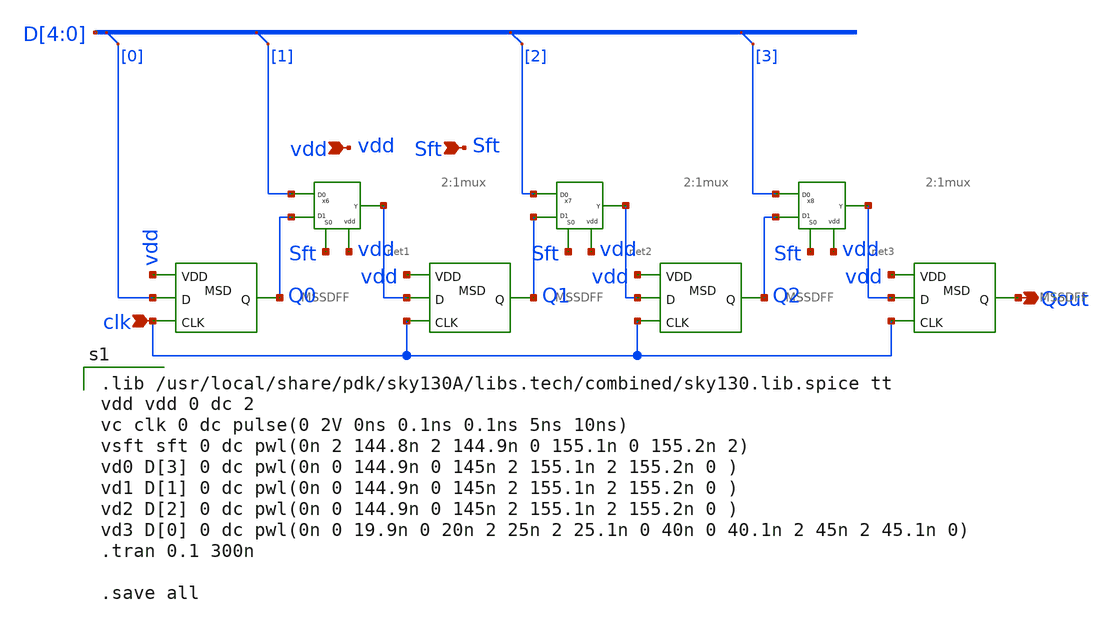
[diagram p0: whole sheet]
** sch_path: Circuit Files/circuits/circuits/AIOSR.sch
**.subckt AIOSR Qout vdd clk Sft
*.opin Qout
*.ipin vdd
*.ipin clk
*.ipin Sft
x1 Q0 vdd D[0] clk MSSDFF
x2 Q1 vdd net1 clk MSSDFF
x3 Q2 vdd net2 clk MSSDFF
x4 Qout vdd net3 clk MSSDFF
x6 D[1] Sft vdd net1 Q0 2:1mux
x7 D[2] Sft vdd net2 Q1 2:1mux
x8 D[3] Sft vdd net3 Q2 2:1mux
* tap: D[4:0] --> D[0]
* tap: D[4:0] --> D[1]
* tap: D[4:0] --> D[2]
* tap: D[4:0] --> D[3]
**** begin user architecture code

.lib /usr/local/share/pdk/sky130A/libs.tech/combined/sky130.lib.spice tt
vdd vdd 0 dc 2
vc clk 0 dc pulse(0 2V 0ns 0.1ns 0.1ns 5ns 10ns)
vsft sft 0 dc pwl(0n 2 144.8n 2 144.9n 0 155.1n 0 155.2n 2)
vd0 D[3] 0 dc pwl(0n 0 144.9n 0 145n 2 155.1n 2 155.2n 0 )
vd1 D[1] 0 dc pwl(0n 0 144.9n 0 145n 2 155.1n 2 155.2n 0 )
vd2 D[2] 0 dc pwl(0n 0 144.9n 0 145n 2 155.1n 2 155.2n 0 )
vd3 D[0] 0 dc pwl(0n 0 19.9n 0 20n 2 25n 2 25.1n 0 40n 0 40.1n 2 45n 2 45.1n 0)
.tran 0.1 300n

.save all


**** end user architecture code
**.ends

* expanding   symbol:  daVLSI_World/circuits/MSSDFF.sym # of pins=4
** sym_path: Circuit Files/circuits/circuits/MSSDFF.sym
** sch_path: Circuit Files/circuits/circuits/MSSDFF.sch
.subckt MSSDFF Q VDD D CLK
*.ipin D
*.opin Q
*.ipin CLK
*.ipin VDD
x2 VDD D net2 CLK DFF1
x1 VDD net2 Q net1 DFF1
x3 net3 net4 net5 inverter_vtc
.ends


* expanding   symbol:  daVLSI_World/circuits/2:1mux.sym # of pins=5
** sym_path: Circuit Files/circuits/circuits/2:1mux.sym
** sch_path: Circuit Files/circuits/circuits/2:1mux.sch
.subckt 2:1mux D0 S0 vdd Y D1
*.ipin vdd
*.ipin D1
*.ipin D0
*.ipin S0
*.opin Y
x1 vdd net3 net1 D0 AND_gate
x2 vdd net1 net2 Y OR_gate
x3 vdd net4 net5 inverter_vtc
x4 vdd S0 net2 D1 AND_gate
.ends


* expanding   symbol:  daVLSI_World/circuits/DFF1.sym # of pins=4
** sym_path: Circuit Files/circuits/circuits/DFF1.sym
** sch_path: Circuit Files/circuits/circuits/DFF1.sch
.subckt DFF1 vdd D Q clk
*.ipin clk
*.ipin D
*.ipin vdd
*.opin Q
x1 vdd net3 D clk GND NAND_gate
x3 vdd Q net3 net1 GND NAND_gate
x4 vdd net4 clk net2 GND NAND_gate
x5 vdd net1 Q net4 GND NAND_gate
x9 net5 net6 net7 inverter_vtc
**** begin user architecture code


.IC V(Q)=0


**** end user architecture code
.ends


* expanding   symbol:  daVLSI_World/gates/inverter_vtc.sym # of pins=3
** sym_path: Circuit Files/Logic gate design using MOSFETS/gates/inverter_vtc.sym
** sch_path: Circuit Files/Logic gate design using MOSFETS/gates/inverter_vtc.sch
.subckt inverter_vtc vdd vin vout
*.ipin vin
*.opin vout
*.ipin vdd
XM1 vout vin GND GND sky130_fd_pr__nfet_01v8 L=0.15 W=1 nf=1 ad='int((nf+1)/2) * W/nf * 0.29' as='int((nf+2)/2) * W/nf * 0.29'
+ pd='2*int((nf+1)/2) * (W/nf + 0.29)' ps='2*int((nf+2)/2) * (W/nf + 0.29)' nrd='0.29 / W' nrs='0.29 / W'
+ sa=0 sb=0 sd=0 mult=1 m=1
XM2 vout vin vdd vdd sky130_fd_pr__pfet_01v8 L=0.15 W=2 nf=1 ad='int((nf+1)/2) * W/nf * 0.29' as='int((nf+2)/2) * W/nf * 0.29'
+ pd='2*int((nf+1)/2) * (W/nf + 0.29)' ps='2*int((nf+2)/2) * (W/nf + 0.29)' nrd='0.29 / W' nrs='0.29 / W'
+ sa=0 sb=0 sd=0 mult=1 m=1
.ends


* expanding   symbol:  daVLSI_World/gates/AND_gate.sym # of pins=4
** sym_path: Circuit Files/Logic gate design using MOSFETS/gates/AND_gate.sym
** sch_path: Circuit Files/Logic gate design using MOSFETS/gates/AND_gate.sch
.subckt AND_gate vdd A Y B
*.opin Y
*.ipin A
*.ipin B
*.ipin vdd
x1 vdd net1 A B GND NAND_gate
x2 vdd net1 Y inverter_vtc
.ends


* expanding   symbol:  daVLSI_World/gates/OR_gate.sym # of pins=4
** sym_path: Circuit Files/Logic gate design using MOSFETS/gates/OR_gate.sym
** sch_path: Circuit Files/Logic gate design using MOSFETS/gates/OR_gate.sch
.subckt OR_gate vdd A B Y
*.ipin A
*.ipin B
*.ipin vdd
*.opin Y
XM1 net1 B net2 vdd sky130_fd_pr__pfet_01v8 L=0.15 W=2 nf=1 ad='int((nf+1)/2) * W/nf * 0.29' as='int((nf+2)/2) * W/nf * 0.29'
+ pd='2*int((nf+1)/2) * (W/nf + 0.29)' ps='2*int((nf+2)/2) * (W/nf + 0.29)' nrd='0.29 / W' nrs='0.29 / W'
+ sa=0 sb=0 sd=0 mult=1 m=1
XM2 net2 A vdd vdd sky130_fd_pr__pfet_01v8 L=0.15 W=2 nf=1 ad='int((nf+1)/2) * W/nf * 0.29' as='int((nf+2)/2) * W/nf * 0.29'
+ pd='2*int((nf+1)/2) * (W/nf + 0.29)' ps='2*int((nf+2)/2) * (W/nf + 0.29)' nrd='0.29 / W' nrs='0.29 / W'
+ sa=0 sb=0 sd=0 mult=1 m=1
XM3 net1 B GND GND sky130_fd_pr__nfet_01v8 L=0.15 W=1 nf=1 ad='int((nf+1)/2) * W/nf * 0.29' as='int((nf+2)/2) * W/nf * 0.29'
+ pd='2*int((nf+1)/2) * (W/nf + 0.29)' ps='2*int((nf+2)/2) * (W/nf + 0.29)' nrd='0.29 / W' nrs='0.29 / W'
+ sa=0 sb=0 sd=0 mult=1 m=1
XM4 net1 A GND GND sky130_fd_pr__nfet_01v8 L=0.15 W=1 nf=1 ad='int((nf+1)/2) * W/nf * 0.29' as='int((nf+2)/2) * W/nf * 0.29'
+ pd='2*int((nf+1)/2) * (W/nf + 0.29)' ps='2*int((nf+2)/2) * (W/nf + 0.29)' nrd='0.29 / W' nrs='0.29 / W'
+ sa=0 sb=0 sd=0 mult=1 m=1
XM9 Y net1 vdd vdd sky130_fd_pr__pfet_01v8 L=0.15 W=2 nf=1 ad='int((nf+1)/2) * W/nf * 0.29' as='int((nf+2)/2) * W/nf * 0.29'
+ pd='2*int((nf+1)/2) * (W/nf + 0.29)' ps='2*int((nf+2)/2) * (W/nf + 0.29)' nrd='0.29 / W' nrs='0.29 / W'
+ sa=0 sb=0 sd=0 mult=1 m=1
XM10 Y net1 GND GND sky130_fd_pr__nfet_01v8 L=0.15 W=1 nf=1 ad='int((nf+1)/2) * W/nf * 0.29' as='int((nf+2)/2) * W/nf * 0.29'
+ pd='2*int((nf+1)/2) * (W/nf + 0.29)' ps='2*int((nf+2)/2) * (W/nf + 0.29)' nrd='0.29 / W' nrs='0.29 / W'
+ sa=0 sb=0 sd=0 mult=1 m=1
.ends


* expanding   symbol:  daVLSI_World/gates/NAND_gate.sym # of pins=5
** sym_path: Circuit Files/Logic gate design using MOSFETS/gates/NAND_gate.sym
** sch_path: Circuit Files/Logic gate design using MOSFETS/gates/NAND_gate.sch
.subckt NAND_gate vdd Y A B gnd
*.ipin A
*.ipin B
*.opin Y
*.ipin vdd
*.ipin gnd
XM1 Y A net1 gnd sky130_fd_pr__nfet_01v8 L=0.15 W=1 nf=1 ad='int((nf+1)/2) * W/nf * 0.29' as='int((nf+2)/2) * W/nf * 0.29'
+ pd='2*int((nf+1)/2) * (W/nf + 0.29)' ps='2*int((nf+2)/2) * (W/nf + 0.29)' nrd='0.29 / W' nrs='0.29 / W'
+ sa=0 sb=0 sd=0 mult=1 m=1
XM2 net1 B gnd gnd sky130_fd_pr__nfet_01v8 L=0.15 W=1 nf=1 ad='int((nf+1)/2) * W/nf * 0.29' as='int((nf+2)/2) * W/nf * 0.29'
+ pd='2*int((nf+1)/2) * (W/nf + 0.29)' ps='2*int((nf+2)/2) * (W/nf + 0.29)' nrd='0.29 / W' nrs='0.29 / W'
+ sa=0 sb=0 sd=0 mult=1 m=1
XM3 Y A vdd vdd sky130_fd_pr__pfet_01v8 L=0.15 W=2 nf=1 ad='int((nf+1)/2) * W/nf * 0.29' as='int((nf+2)/2) * W/nf * 0.29'
+ pd='2*int((nf+1)/2) * (W/nf + 0.29)' ps='2*int((nf+2)/2) * (W/nf + 0.29)' nrd='0.29 / W' nrs='0.29 / W'
+ sa=0 sb=0 sd=0 mult=1 m=1
XM4 Y B vdd vdd sky130_fd_pr__pfet_01v8 L=0.15 W=2 nf=1 ad='int((nf+1)/2) * W/nf * 0.29' as='int((nf+2)/2) * W/nf * 0.29'
+ pd='2*int((nf+1)/2) * (W/nf + 0.29)' ps='2*int((nf+2)/2) * (W/nf + 0.29)' nrd='0.29 / W' nrs='0.29 / W'
+ sa=0 sb=0 sd=0 mult=1 m=1
.ends

.GLOBAL GND
.end
